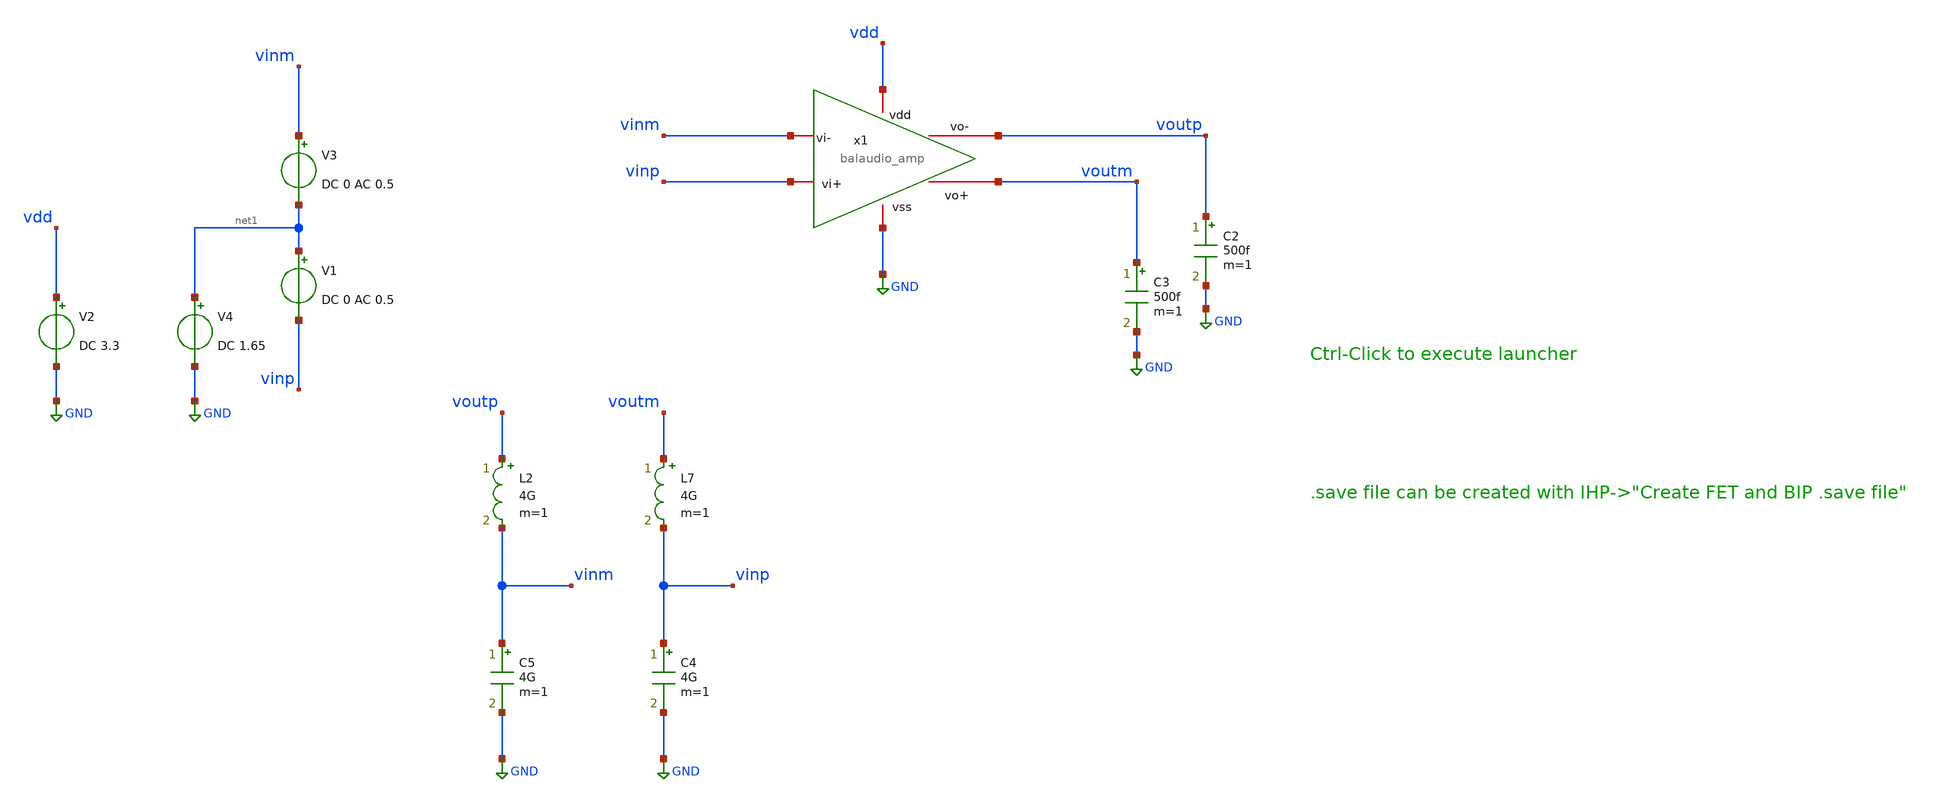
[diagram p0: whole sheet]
** sch_path: testbench/balaudio_amp_tb.sch
**.subckt balaudio_amp_tb
C2 voutp GND 500f m=1
V2 vdd GND DC 3.3
V1 net1 vinp DC 0 AC 0.5
V3 vinm net1 DC 0 AC 0.5
V4 net1 GND DC 1.65
L2 voutp vinm 4G m=1
L7 voutm vinp 4G m=1
x1 vdd vinm vinp voutm voutp GND balaudio_amp
C3 voutm GND 500f m=1
C4 vinp GND 4G m=1
C5 vinm GND 4G m=1
**** begin user architecture code

.lib cornerMOShv.lib mos_tt
.lib $::SG13G2_MODELS/cornerCAP.lib cap_typ



.param temp=27
.include balaudio_amp_tb.save
.control

* --- OP ---
op
save all
write balaudio_amp_tb.raw
set appendwrite

* --- DC Sweep ---
tran 10u 10m
save all

* --- AC Sweep ---
ac dec 100 10 100e6
save all

let Av = db(v(voutp))
let Phase = 180/3.14*vp(voutp) - 180
let CMRR = db((v(voutp)/v(vinp))/(v(voutp_cmrr)/v(vinp)))
let PSRR = db(v(voutp_psrr)/v(vdd_ac))

echo ---
meas ac gm_db find vdb(voutp) when vp(voutp)=0
meas ac pm_deg find Phase when vdb(voutp)=0
meas ac _3db_f when Phase=-45
meas ac _0db_f when vdb(voutp)=0
meas ac dc_gain find vdb(voutp) at=10
echo ---

write balaudio_amp_tb.raw
.endc


**** end user architecture code
**.ends

* expanding   symbol:  balaudio_amp.sym # of pins=6
** sym_path: schematic/balaudio_amp.sym
** sch_path: schematic/balaudio_amp.sch
.subckt balaudio_amp vdd vi- vi+ vo+ vo- vss
*.iopin vdd
*.iopin vss
*.iopin vi+
*.iopin vi-
*.iopin vo-
*.iopin vo+
XM4 A2_vi+ nmirror vss vss sg13_hv_nmos w=0.3u l=0.45u ng=1 m=1 mm_ok=1
XM1 A2_vi- vi- net1 vdd sg13_hv_pmos w=0.3u l=0.4u ng=1 m=1 mm_ok=1
XM2 A2_vi+ vi+ net1 vdd sg13_hv_pmos w=0.3u l=0.4u ng=1 m=1 mm_ok=1
XM3 net1 vb_tail vdd vdd sg13_hv_pmos w=0.3u l=0.4u ng=1 m=1 mm_ok=1
XM5 A2_vi- nmirror vss vss sg13_hv_nmos w=0.3u l=0.45u ng=1 m=1 mm_ok=1
XM6 vo- A2_vo- A2_vi+ vss sg13_hv_nmos w=0.3u l=0.45u ng=1 m=1 mm_ok=1
XM7 vo+ A2_vo+ A2_vi- vss sg13_hv_nmos w=0.3u l=0.45u ng=1 m=1 mm_ok=1
XM10 A1_vi+ vb_p vdd vdd sg13_hv_pmos w=0.3u l=0.4u ng=1 m=1 mm_ok=1
XM11 A1_vi- vb_p vdd vdd sg13_hv_pmos w=0.3u l=0.4u ng=1 m=1 mm_ok=1
XM8 vo- A1_vo- A1_vi+ vdd sg13_hv_pmos w=0.3u l=0.4u ng=1 m=1 mm_ok=1
XM9 vo+ A1_vo+ A1_vi- vdd sg13_hv_pmos w=0.3u l=0.4u ng=1 m=1 mm_ok=1
x1 vdd A1_vi+ A1_vi- A1_vo+ A1_vo- vss A1_cm aux_amp
x2 vdd A2_vi+ A2_vi- A2_vo+ A2_vo- vss A2_cm aux_amp
XM12 vb_tail vb_tail vdd vdd sg13_hv_pmos w=0.3u l=0.4u ng=1 m=1 mm_ok=1
I0 vb_tail vss 10u
V1 vb_p vss 2.0
XM13 nmirror nmirror vss vss sg13_hv_nmos w=0.3u l=0.45u ng=1 m=1 mm_ok=1
I1 vdd nmirror 10u
V2 A1_cm vss 1.65
V3 A2_cm vss 1.65
.ends


* expanding   symbol:  aux_amp.sym # of pins=7
** sym_path: schematic/aux_amp.sym
** sch_path: schematic/aux_amp.sch
.subckt aux_amp vdd vi- vi+ vo+ vo- vss cm_in
*.iopin vss
*.iopin vo-
*.iopin vdd
*.iopin vo+
*.iopin vi-
*.iopin vi+
*.iopin cm_in
XM1 net3 vi+ net1 net1 sg13_hv_nmos w=80.0u l=10.0u ng=8 m=1 mm_ok=1
XM2 net4 cm_in net1 net1 sg13_hv_nmos w=80.0u l=10.0u ng=8 m=1 mm_ok=1
XM5 net1 nbias vss vss sg13_hv_nmos w=60.0u l=10.0u ng=8 m=1 mm_ok=1
XM3 net3 cm_in net2 net2 sg13_hv_nmos w=80.0u l=10.0u ng=8 m=1 mm_ok=1
XM4 net4 vi- net2 net2 sg13_hv_nmos w=80.0u l=10.0u ng=8 m=1 mm_ok=1
XM6 net2 nbias vss vss sg13_hv_nmos w=60.0u l=10.0u ng=8 m=1 mm_ok=1
XM11 vo- nbias vss vss sg13_hv_nmos w=29.0u l=10.0u ng=8 m=1 mm_ok=1
XM12 vo+ nbias vss vss sg13_hv_nmos w=29.0u l=10.0u ng=8 m=1 mm_ok=1
V3 pbias vss 1.80
XM9 vo- pbias net3 net3 sg13_hv_pmos w=15.0u l=2.0u ng=8 m=1 mm_ok=1
XM7 net3 pbias_top vdd vdd sg13_hv_pmos w=4.0u l=1.0u ng=1 m=1 mm_ok=1
XM8 net4 pbias_top vdd vdd sg13_hv_pmos w=4.0u l=1.0u ng=1 m=1 mm_ok=1
XM10 vo+ pbias net4 net4 sg13_hv_pmos w=15.0u l=2.0u ng=8 m=1 mm_ok=1
XM14 nbias nbias vss vss sg13_hv_nmos w=29.0u l=10.0u ng=8 m=1 mm_ok=1
I1 vdd nbias 1.0u
V1 pbias_top vss 2.2
.ends

.GLOBAL GND
.end
